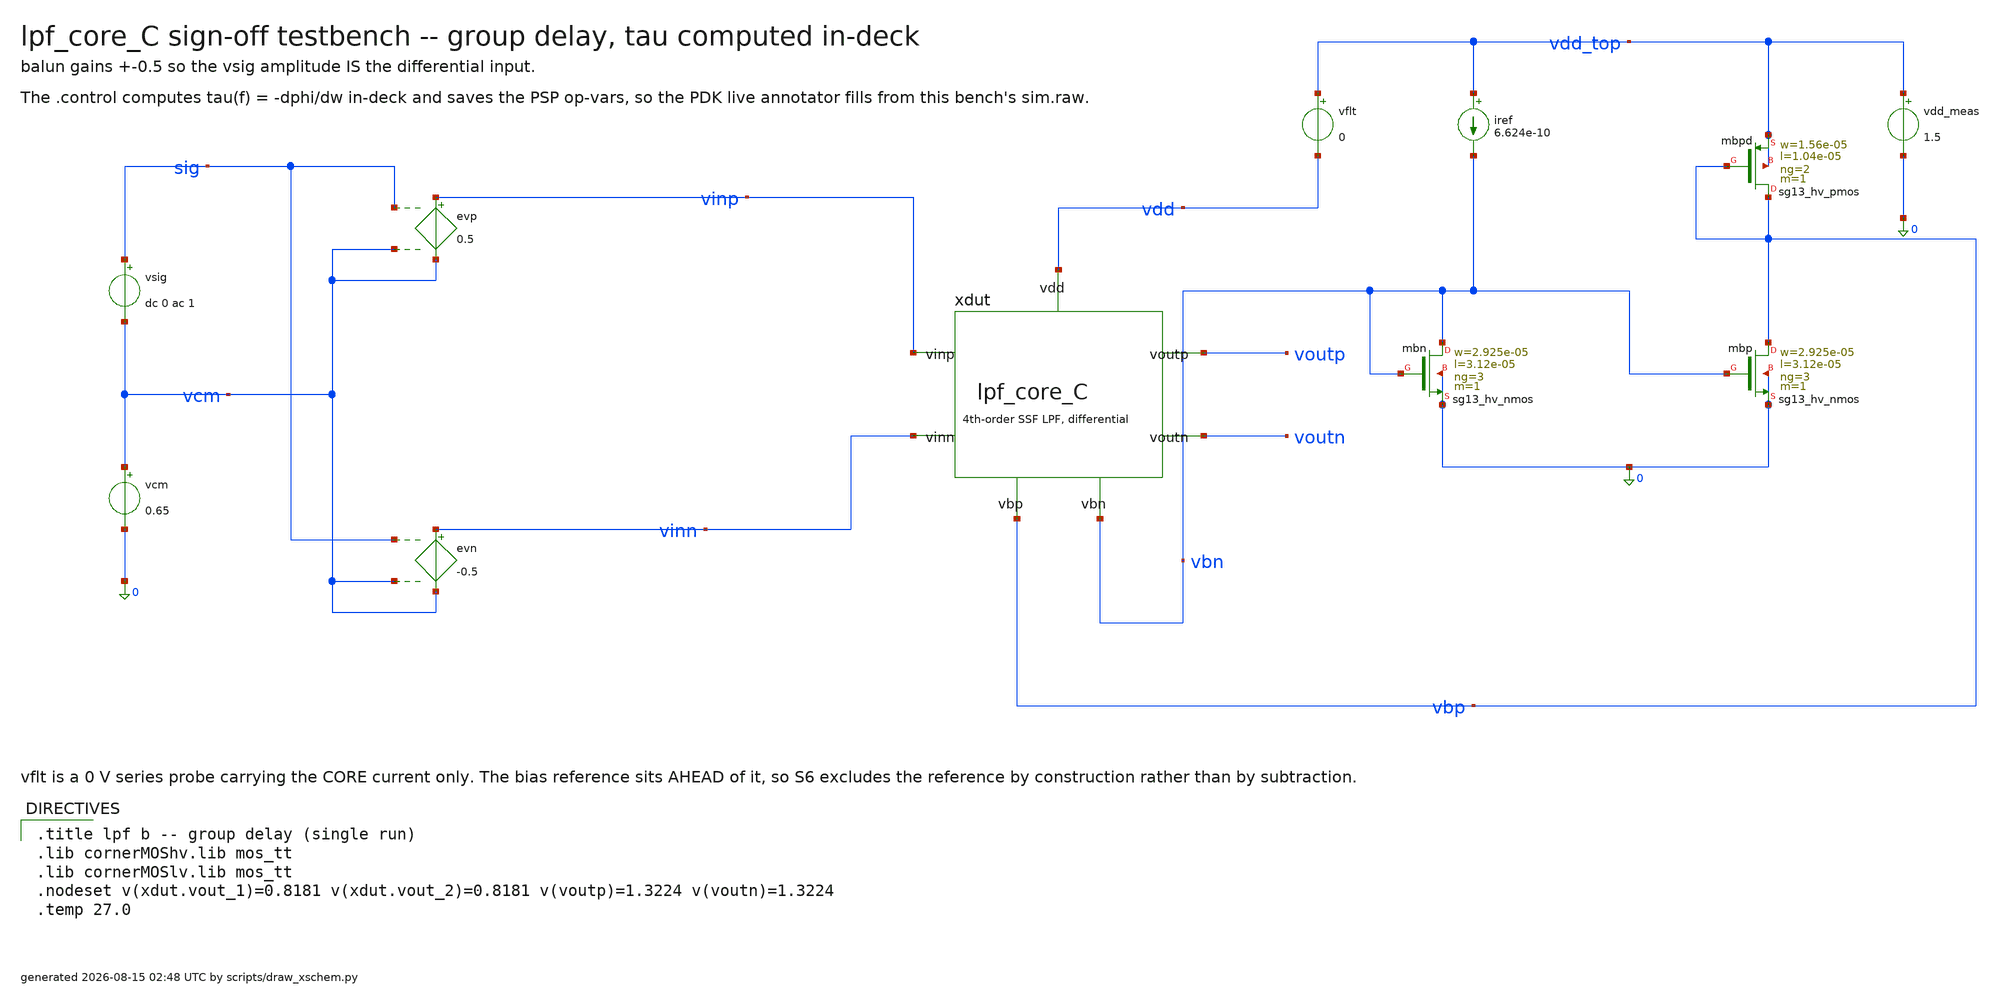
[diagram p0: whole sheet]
** sch_path: signoff/C-lownoise/lpf_tb_C_gd.sch
**.subckt lpf_tb_C_gd
vsig sig vcm dc 0 ac 1
vcm vcm 0 0.65
evp vinp vcm sig vcm 0.5
evn vinn vcm sig vcm -0.5
xdut vinp vinn voutp voutn vbn vbp vdd lpf_core_C
vflt vdd_top vdd 0
vdd_meas vdd_top 0 1.5
iref vdd_top vbn 6.624e-10
Xmbn vbn vbn 0 0 sg13_hv_nmos w=2.925e-05 l=3.12e-05 ng=3 m=1 mm_ok=1
Xmbp vbp vbn 0 0 sg13_hv_nmos w=2.925e-05 l=3.12e-05 ng=3 m=1 mm_ok=1
Xmbpd vbp vbp vdd_top vdd_top sg13_hv_pmos w=1.56e-05 l=1.04e-05 ng=2 m=1 mm_ok=1
**** begin user architecture code

.title lpf b -- group delay (single run)
.lib cornerMOShv.lib mos_tt
.lib cornerMOSlv.lib mos_tt
.nodeset v(xdut.vout_1)=0.8181 v(xdut.vout_2)=0.8181 v(voutp)=1.3224 v(voutn)=1.3224
.temp 27.0


.control
set filetype=binary
set appendwrite
save all @n.xdut.xm2.nsg13_lv_pmos[ids] @n.xdut.xm2.nsg13_lv_pmos[gm] @n.xdut.xm2.nsg13_lv_pmos[gds]
+ @n.xdut.xm2.nsg13_lv_pmos[gmb] @n.xdut.xm2.nsg13_lv_pmos[vgs] @n.xdut.xm2.nsg13_lv_pmos[vds] @n.xdut.xm2.nsg13_lv_pmos[vth]
+ @n.xdut.xm2.nsg13_lv_pmos[vdss] @n.xdut.xm2.nsg13_lv_pmos[cgg] @n.xdut.xm5.nsg13_lv_pmos[ids] @n.xdut.xm5.nsg13_lv_pmos[gm]
+ @n.xdut.xm5.nsg13_lv_pmos[gds] @n.xdut.xm5.nsg13_lv_pmos[gmb] @n.xdut.xm5.nsg13_lv_pmos[vgs] @n.xdut.xm5.nsg13_lv_pmos[vds]
+ @n.xdut.xm5.nsg13_lv_pmos[vth] @n.xdut.xm5.nsg13_lv_pmos[vdss] @n.xdut.xm5.nsg13_lv_pmos[cgg] @n.xdut.xm4.nsg13_hv_nmos[ids]
+ @n.xdut.xm4.nsg13_hv_nmos[gm] @n.xdut.xm4.nsg13_hv_nmos[gds] @n.xdut.xm4.nsg13_hv_nmos[gmb] @n.xdut.xm4.nsg13_hv_nmos[vgs]
+ @n.xdut.xm4.nsg13_hv_nmos[vds] @n.xdut.xm4.nsg13_hv_nmos[vth] @n.xdut.xm4.nsg13_hv_nmos[vdss] @n.xdut.xm4.nsg13_hv_nmos[cgg]
+ @n.xdut.xm8.nsg13_hv_nmos[ids] @n.xdut.xm8.nsg13_hv_nmos[gm] @n.xdut.xm8.nsg13_hv_nmos[gds] @n.xdut.xm8.nsg13_hv_nmos[gmb]
+ @n.xdut.xm8.nsg13_hv_nmos[vgs] @n.xdut.xm8.nsg13_hv_nmos[vds] @n.xdut.xm8.nsg13_hv_nmos[vth] @n.xdut.xm8.nsg13_hv_nmos[vdss]
+ @n.xdut.xm8.nsg13_hv_nmos[cgg] @n.xdut.xm9.nsg13_hv_nmos[ids] @n.xdut.xm9.nsg13_hv_nmos[gm] @n.xdut.xm9.nsg13_hv_nmos[gds]
+ @n.xdut.xm9.nsg13_hv_nmos[gmb] @n.xdut.xm9.nsg13_hv_nmos[vgs] @n.xdut.xm9.nsg13_hv_nmos[vds] @n.xdut.xm9.nsg13_hv_nmos[vth]
+ @n.xdut.xm9.nsg13_hv_nmos[vdss] @n.xdut.xm9.nsg13_hv_nmos[cgg] @n.xdut.xm10.nsg13_hv_nmos[ids] @n.xdut.xm10.nsg13_hv_nmos[gm]
+ @n.xdut.xm10.nsg13_hv_nmos[gds] @n.xdut.xm10.nsg13_hv_nmos[gmb] @n.xdut.xm10.nsg13_hv_nmos[vgs] @n.xdut.xm10.nsg13_hv_nmos[vds]
+ @n.xdut.xm10.nsg13_hv_nmos[vth] @n.xdut.xm10.nsg13_hv_nmos[vdss] @n.xdut.xm10.nsg13_hv_nmos[cgg] @n.xdut.xmst.nsg13_hv_pmos[ids]
+ @n.xdut.xmst.nsg13_hv_pmos[gm] @n.xdut.xmst.nsg13_hv_pmos[gds] @n.xdut.xmst.nsg13_hv_pmos[gmb] @n.xdut.xmst.nsg13_hv_pmos[vgs]
+ @n.xdut.xmst.nsg13_hv_pmos[vds] @n.xdut.xmst.nsg13_hv_pmos[vth] @n.xdut.xmst.nsg13_hv_pmos[vdss] @n.xdut.xmst.nsg13_hv_pmos[cgg]
+ @n.xdut.xmstn.nsg13_hv_pmos[ids] @n.xdut.xmstn.nsg13_hv_pmos[gm] @n.xdut.xmstn.nsg13_hv_pmos[gds] @n.xdut.xmstn.nsg13_hv_pmos[gmb]
+ @n.xdut.xmstn.nsg13_hv_pmos[vgs] @n.xdut.xmstn.nsg13_hv_pmos[vds] @n.xdut.xmstn.nsg13_hv_pmos[vth] @n.xdut.xmstn.nsg13_hv_pmos[vdss]
+ @n.xdut.xmstn.nsg13_hv_pmos[cgg] @n.xdut.xm0.nsg13_hv_pmos[ids] @n.xdut.xm0.nsg13_hv_pmos[gm] @n.xdut.xm0.nsg13_hv_pmos[gds]
+ @n.xdut.xm0.nsg13_hv_pmos[gmb] @n.xdut.xm0.nsg13_hv_pmos[vgs] @n.xdut.xm0.nsg13_hv_pmos[vds] @n.xdut.xm0.nsg13_hv_pmos[vth]
+ @n.xdut.xm0.nsg13_hv_pmos[vdss] @n.xdut.xm0.nsg13_hv_pmos[cgg] @n.xdut.xm1.nsg13_hv_pmos[ids] @n.xdut.xm1.nsg13_hv_pmos[gm]
+ @n.xdut.xm1.nsg13_hv_pmos[gds] @n.xdut.xm1.nsg13_hv_pmos[gmb] @n.xdut.xm1.nsg13_hv_pmos[vgs] @n.xdut.xm1.nsg13_hv_pmos[vds]
+ @n.xdut.xm1.nsg13_hv_pmos[vth] @n.xdut.xm1.nsg13_hv_pmos[vdss] @n.xdut.xm1.nsg13_hv_pmos[cgg] @n.xdut.xm14.nsg13_hv_pmos[ids]
+ @n.xdut.xm14.nsg13_hv_pmos[gm] @n.xdut.xm14.nsg13_hv_pmos[gds] @n.xdut.xm14.nsg13_hv_pmos[gmb] @n.xdut.xm14.nsg13_hv_pmos[vgs]
+ @n.xdut.xm14.nsg13_hv_pmos[vds] @n.xdut.xm14.nsg13_hv_pmos[vth] @n.xdut.xm14.nsg13_hv_pmos[vdss] @n.xdut.xm14.nsg13_hv_pmos[cgg]
+ @n.xdut.xm15.nsg13_hv_pmos[ids] @n.xdut.xm15.nsg13_hv_pmos[gm] @n.xdut.xm15.nsg13_hv_pmos[gds] @n.xdut.xm15.nsg13_hv_pmos[gmb]
+ @n.xdut.xm15.nsg13_hv_pmos[vgs] @n.xdut.xm15.nsg13_hv_pmos[vds] @n.xdut.xm15.nsg13_hv_pmos[vth] @n.xdut.xm15.nsg13_hv_pmos[vdss]
+ @n.xdut.xm15.nsg13_hv_pmos[cgg]
op
write sim.raw
ac dec 50 0.1 1000
let hdiff = v(voutp) - v(voutn)
let hdb = db(mag(hdiff))
let dc_db = hdb[0]
let ph = cph(hdiff)
let gd = -deriv(ph) / (2 * pi)
let gd_dc_ms = gd[0] * 1e3
let gd_max_ms = vecmax(gd) * 1e3
let hrel = hdb - dc_db
meas ac fc_hz when hrel = -3 fall = 1
print dc_db gd_dc_ms gd_max_ms
write sim.raw hdiff ph gd frequency
.endc

**** end user architecture code
**.ends
.end
